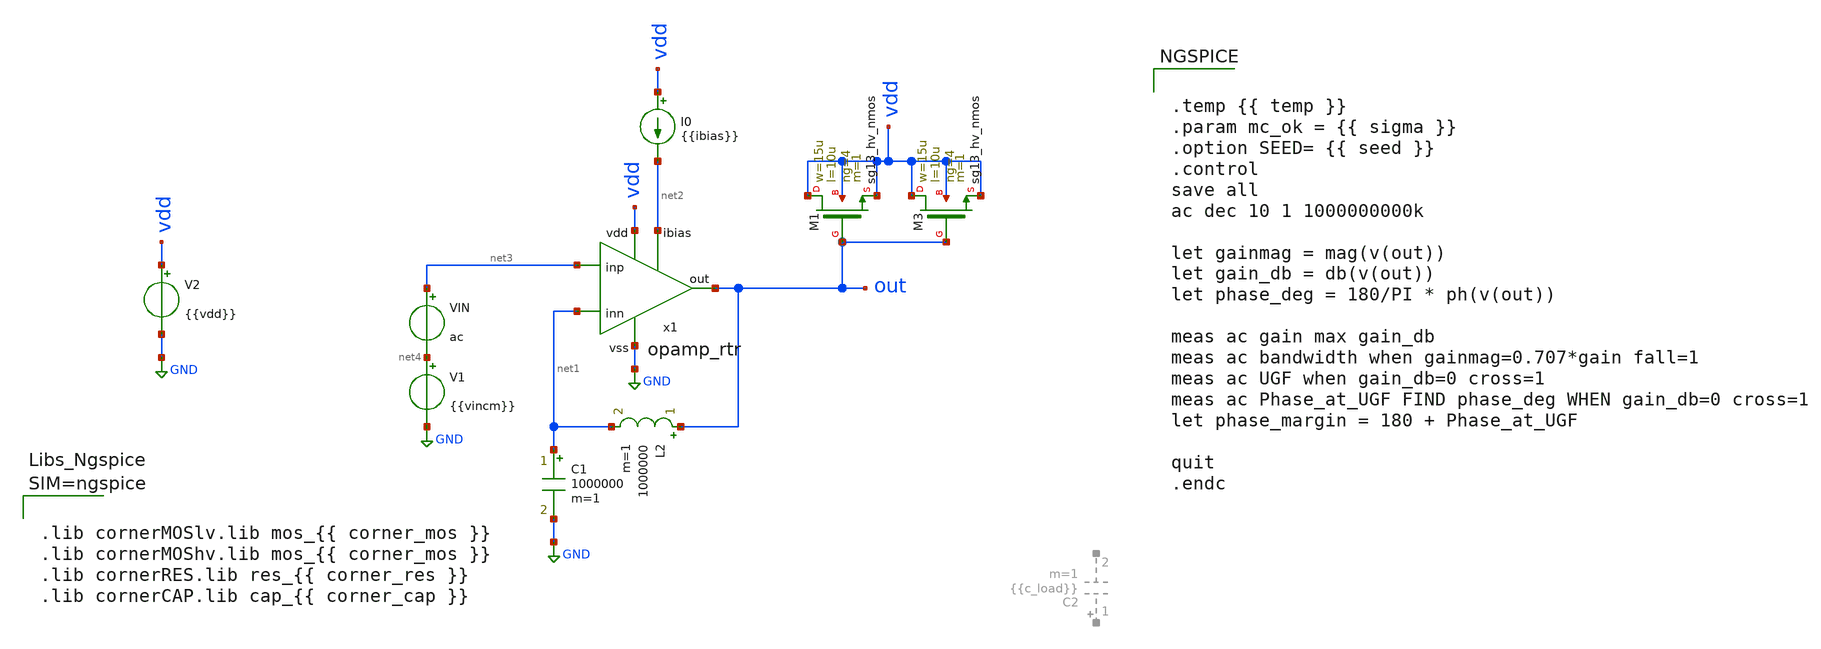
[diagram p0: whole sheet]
** sch_path: testbenches/xschem/tb_opamp_rtr_gain.sch
**.subckt tb_opamp_rtr_gain
V1 net4 GND {{vincm}}
.save i(v1)
V2 vdd GND {{vdd}}
VIN net3 net4 ac
.save i(vin)
L2 out net1 1000000 m=1
C1 net1 GND 1000000 m=1
I0 vdd net2 {{ibias}}
XM3 vdd out vdd vdd sg13_hv_nmos w=15u l=10u ng=4 m=1 mm_ok=1
XM1 vdd out vdd vdd sg13_hv_nmos w=15u l=10u ng=4 m=1 mm_ok=1
x1 vdd net3 GND net1 net2 out opamp_rtr
**** begin user architecture code


.temp {{ temp }}
.param mc_ok = {{ sigma }}
.option SEED= {{ seed }}
.control
save all
ac dec 10 1 1000000000k

let gainmag = mag(v(out))
let gain_db = db(v(out))
let phase_deg = 180/PI * ph(v(out))

meas ac gain max gain_db
meas ac bandwidth when gainmag=0.707*gain fall=1
meas ac UGF when gain_db=0 cross=1
meas ac Phase_at_UGF FIND phase_deg WHEN gain_db=0 cross=1
let phase_margin = 180 + Phase_at_UGF

quit
.endc





.lib cornerMOSlv.lib mos_{{ corner_mos }}
.lib cornerMOShv.lib mos_{{ corner_mos }}
.lib cornerRES.lib res_{{ corner_res }}
.lib cornerCAP.lib cap_{{ corner_cap }}



**** end user architecture code
**.ends

* expanding   symbol:  heichip/opamp_rtr/schematic/xschem/opamp_rtr.sym # of pins=6
** sym_path: schematic/xschem/opamp_rtr.sym
** sch_path: schematic/xschem/opamp_rtr.sch
.subckt opamp_rtr vdd inp vss inn ibias out
*.ipin inp
*.opin out
*.iopin vdd
*.ipin inn
*.ipin ibias
*.iopin vss
XXM6 out1_n inp ncmdiff_n vss sg13_hv_nmos w={w_diff_n} l={l_diff} ng={n_diff_n} m=1 mm_ok=1
XXM1 net1 inn ncmdiff_p vdd sg13_hv_pmos w={w_diff_p} l={l_diff} ng={n_diff_p} m=1 mm_ok=1
XXM2 ncmdiff_p inp out1_p vdd sg13_hv_pmos w={w_diff_p} l={l_diff} ng={n_diff_p} m=1 mm_ok=1
XXM3 ncmdiff_p vbias_p vdd vdd sg13_hv_pmos w={w_tail_p} l={l_bias} ng={n_tail_p} m=1 mm_ok=1
XXM4 vss net1 net1 vss sg13_hv_nmos w={w_load_n} l={l_load} ng={n_load_n} m=1 mm_ok=1
XXM5 out1_p net1 vss vss sg13_hv_nmos w={w_load_n} l={l_load} ng={n_load_n} m=1 mm_ok=1
XXM7 ncmdiff_n inn net2 vss sg13_hv_nmos w={w_diff_n} l={l_diff} ng={n_diff_n} m=1 mm_ok=1
XXM8 ncmdiff_n ibias vss vss sg13_hv_nmos w={w_tail_n} l={l_bias} ng={n_tail_n} m=1 mm_ok=1
XXM9 vdd net2 out1_n vdd sg13_hv_pmos w={w_load_p} l={l_load} ng={n_load_p} m=1 mm_ok=1
XXM10 net2 net2 vdd vdd sg13_hv_pmos w={w_load_p} l={l_load} ng={n_load_p} m=1 mm_ok=1
XXM25 nswa vref_p ncmdiff_p ncmdiff_p sg13_hv_pmos w={w_sw_p} l={l_sw} ng={n_sw_p} m=1 mm_ok=1
XXM26 nswa nswa vss vss sg13_hv_nmos w={w_gmn} l={l_bias} ng={n_gmn} m=1 mm_ok=1
XXM27 ncmdiff_n nswa vss vss sg13_hv_nmos w={w_gmn} l={l_bias} ng={n_gmn} m=1 mm_ok=1
XXM28 ncmdiff_n vref_n nswb vss sg13_hv_nmos w={w_sw_n} l={l_sw} ng={n_sw_n} m=1 mm_ok=1
XXM29 nswb nswb vdd vdd sg13_hv_pmos w={w_gmp} l={l_bias} ng={n_gmp} m=1 mm_ok=1
XXM30 ncmdiff_p nswb vdd vdd sg13_hv_pmos w={w_gmp} l={l_bias} ng={n_gmp} m=1 mm_ok=1
XXM13 out1_n nabn out1_p vss sg13_hv_nmos w={w_ab_n} l={l_ab} ng={n_ab_n} m=1 mm_ok=1
XXM14 out1_p nabp out1_n vdd sg13_hv_pmos w={w_ab_p} l={l_ab} ng={n_ab_p} m=1 mm_ok=1
XXM15 out1_n vbias_p vdd vdd sg13_hv_pmos w={w_ab_src} l={l_bias} ng={n_ab_src} m=1 mm_ok=1
XXM16 out1_p nab_ref vss vss sg13_hv_nmos w={w_ab_snk} l={l_bias} ng={n_ab_snk} m=1 mm_ok=1
XXM23 nab_ref vbias_p vdd vdd sg13_hv_pmos w={w_ab_src} l={l_bias} ng={n_ab_src} m=1 mm_ok=1
XXM24 nab_ref nab_ref vss vss sg13_hv_nmos w={w_ab_snk} l={l_bias} ng={n_ab_snk} m=1 mm_ok=1
XXM17 nabn vbias_p vdd vdd sg13_hv_pmos w={w_ab_src} l={l_bias} ng={n_ab_src} m=1 mm_ok=1
XXM18 nabn nabn net3 vss sg13_hv_nmos w={w_ab_n} l={l_ab} ng={n_ab_n} m=1 mm_ok=1
XXM19 net3 net3 vss vss sg13_hv_nmos w={w_ab_n} l={l_ab} ng={n_ab_n} m=1 mm_ok=1
XXM20 nabp nab_ref vss vss sg13_hv_nmos w={w_ab_snk} l={l_bias} ng={n_ab_snk} m=1 mm_ok=1
XXM21 nabp nabp net4 vdd sg13_hv_pmos w={w_ab_p} l={l_ab} ng={n_ab_p} m=1 mm_ok=1
XXM22 net4 net4 vdd vdd sg13_hv_pmos w={w_ab_p} l={l_ab} ng={n_ab_p} m=1 mm_ok=1
XXM11 out out1_n vdd vdd sg13_hv_pmos w={w_out_p} l={l_out} ng={n_out_p} m=1 mm_ok=1
XXM12 out out1_p vss vss sg13_hv_nmos w={w_out_n} l={l_out} ng={n_out_n} m=1 mm_ok=1
XXB1 ibias ibias vss vss sg13_hv_nmos w={w_bias_n} l={l_bias} ng={n_bias_n} m=1 mm_ok=1
XXB2 vbias_p ibias vss vss sg13_hv_nmos w={w_bias_n} l={l_bias} ng={n_bias_n} m=1 mm_ok=1
XXB5 vref_n vref_n vss vss sg13_hv_nmos w={w_ref_n} l={l_bias} ng={n_ref_n} m=1 mm_ok=1
XXB6 vref_p ibias vss vss sg13_hv_nmos w={w_bias_n} l={l_bias} ng={n_bias_n} m=1 mm_ok=1
XXB3 vbias_p vbias_p vdd vdd sg13_hv_pmos w={w_bias_p} l={l_bias} ng={n_bias_p} m=1 mm_ok=1
XXB4 vref_n vbias_p vdd vdd sg13_hv_pmos w={w_bias_p} l={l_bias} ng={n_bias_p} m=1 mm_ok=1
XXB7 vref_p vref_p vdd vdd sg13_hv_pmos w={w_ref_p} l={l_bias} ng={n_ref_p} m=1 mm_ok=1
**** begin user architecture code


*bias network
.param l_bias=4u
.param w_bias_p=15u
.param n_bias_p=4
.param w_bias_n=5u
.param n_bias_n=5
.param w_ref_n=5u
.param n_ref_n=4
.param w_ref_p=15u
.param n_ref_p=4
*first stage
.param l_diff=2u
.param l_load=4u

.param w_diff_n=5u
.param n_diff_n=4

.param w_diff_p=15u
.param n_diff_p=4

.param w_load_n=5u
.param n_load_n=4

.param w_load_p=15u
.param n_load_p=4

.param w_tail_n=5u
.param n_tail_n=4

.param w_tail_p=15u
.param n_tail_p=4

.param l_sw=1u
.param w_sw_p=15u
.param n_sw_p=4

.param w_sw_n=5u
.param n_sw_n=4

.param w_gmn=5u
.param n_gmn=4

.param w_gmp=15u
.param n_gmp=4

*output control circuit
.param w_ab_src=15u
.param n_ab_src=4
.param w_ab_snk=5u
.param n_ab_snk=4

.param w_ab_n=5u
.param n_ab_n=4
.param w_ab_p=15u
.param n_ab_p=4

.param l_ab=1u

.param w_out_p=60u
.param n_out_p=4
.param w_out_n=20u
.param n_out_n=4
.param l_out=1u

.param r_null=50k
.param c_null=500f



**** end user architecture code
XC3 out net5 cap_cmomf w=13.5e-6 l=21e-6 mmin=1 mmax=4 subblock=0 m=1 mm_ok=1
XC2 out net6 cap_cmomf w=13.5e-6 l=21e-6 mmin=1 mmax=4 subblock=0 m=1 mm_ok=1
XR4 net5 out1_n vss rhigh w=1e-6 l=36e-6 m=1 b=0 mm_ok=1
XR2 net6 out1_p vss rhigh w=1e-6 l=36e-6 m=1 b=0 mm_ok=1
XDUMMY1 ncmdiff_n ncmdiff_n ncmdiff_n vss sg13_hv_nmos w=5u l=0.45u ng=4 m=1 mm_ok=1
XDUMMY2 ncmdiff_n ncmdiff_n ncmdiff_n vss sg13_hv_nmos w=5u l=0.45u ng=2 m=1 mm_ok=1
XDUMMY3 vss vss vss vss sg13_hv_nmos w=7.5u l=0.45u ng=6 m=1 mm_ok=1
XDUMMY4 vss vss vss vss sg13_hv_nmos w=10u l=0.45u ng=4 m=1 mm_ok=1
XDUMMY5 out1_p out1_p out1_p vss sg13_hv_nmos w=5u l=1u ng=2 m=1 mm_ok=1
XDUMMY6 vdd vdd vdd vdd sg13_hv_pmos w=22.5u l=0.4u ng=6 m=1 mm_ok=1
XDUMMY7 nswa nswa nswa vdd sg13_hv_pmos w=15u l=0.4u ng=2 m=1 mm_ok=1
XDUMMY8 vdd vdd vdd vdd sg13_hv_pmos w=15u l=0.4u ng=4 m=1 mm_ok=1
XDUMMY9 vdd vdd vdd vdd sg13_hv_pmos w=37.5u l=0.4u ng=5 m=1 mm_ok=1
XDUMMY10 out1_n out1_n out1_n vdd sg13_hv_pmos w=15u l=0.4u ng=2 m=1 mm_ok=1
XDUMMY11 vss vss vss vss sg13_hv_nmos w=5u l=0.45u ng=2 m=1 mm_ok=1
XR3 vss vss vss rhigh w=1e-6 l=18e-6 m=1 b=0 mm_ok=1
.ends

.GLOBAL GND
.end
